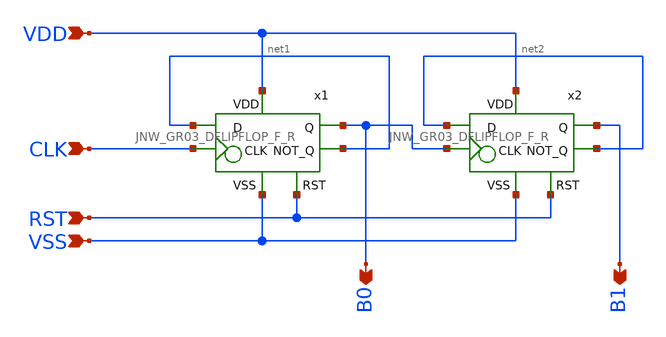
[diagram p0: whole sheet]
** sch_path: design/JNW_GR03_SKY130A/JNW_GR03_2BCOUNTER_R.sch
**.subckt JNW_GR03_2BCOUNTER_R VDD VSS RST CLK B0 B1
*.ipin VDD
*.ipin VSS
*.ipin RST
*.ipin CLK
*.opin B0
*.opin B1
x1 VDD B0 net1 CLK net1 RST VSS JNW_GR03_DFLIPFLOP_F_R
x2 VDD B1 net2 B0 net2 RST VSS JNW_GR03_DFLIPFLOP_F_R
**.ends
.end
